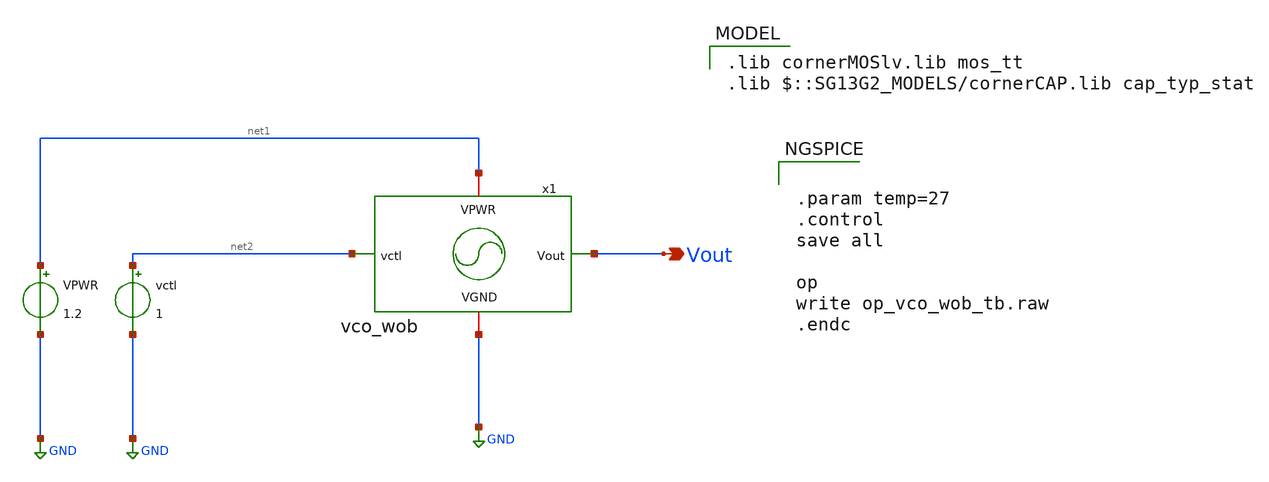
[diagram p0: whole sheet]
** sch_path: Combined_Design/design_data/xschem/vco_wob_tb.sch
**.subckt vco_wob_tb Vout
*.opin Vout
VPWR net1 GND 1.2
vctl net2 GND 1
x1 net1 GND net2 Vout vco_wob
**** begin user architecture code
 .lib cornerMOSlv.lib mos_tt
.lib $::SG13G2_MODELS/cornerCAP.lib cap_typ_stat



.param temp=27
.control
save all

op
write op_vco_wob_tb.raw
.endc


**** end user architecture code
**.ends
.GLOBAL GND
.end
